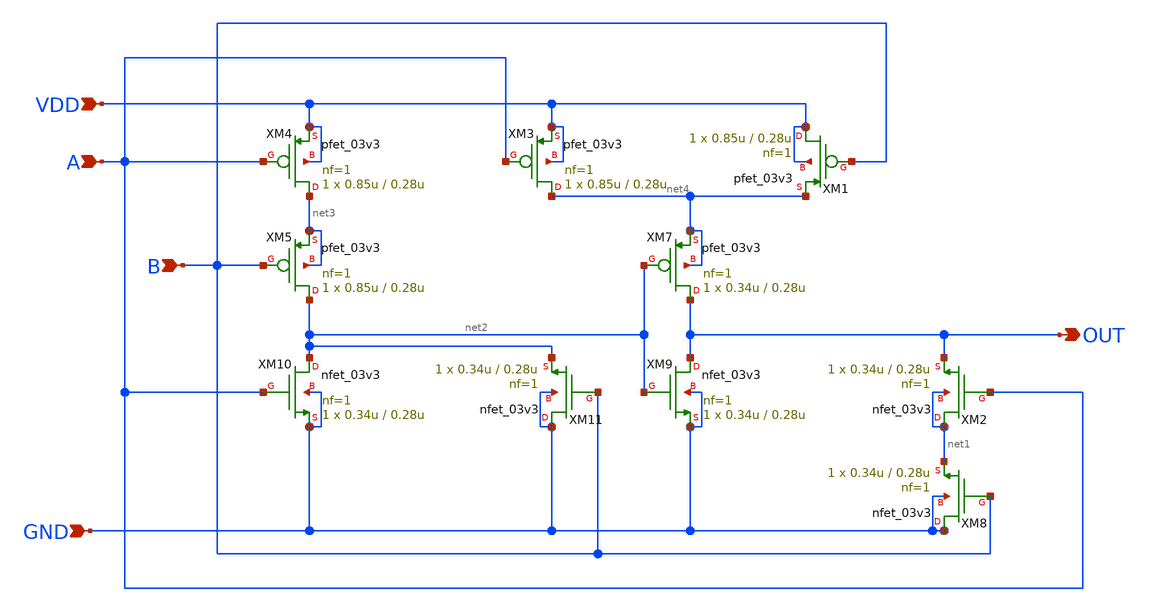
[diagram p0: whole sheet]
** sch_path: Project/1-on-chip/schematic/PNgen/xor.sch
**.subckt xor VDD OUT A B GND
*.ipin VDD
*.opin OUT
*.ipin A
*.ipin B
*.ipin GND
XM7 OUT net2 net4 net4 pfet_03v3 L=0.28u W=0.34u nf=1 ad='int((nf+1)/2) * W/nf * 0.18u' as='int((nf+2)/2) * W/nf * 0.18u'
+ pd='2*int((nf+1)/2) * (W/nf + 0.18u)' ps='2*int((nf+2)/2) * (W/nf + 0.18u)' nrd='0.18u / W' nrs='0.18u / W'
+ sa=0 sb=0 sd=0 m=1
XM1 VDD B net4 VDD pfet_03v3 L=0.28u W=0.85u nf=1 ad='int((nf+1)/2) * W/nf * 0.18u' as='int((nf+2)/2) * W/nf * 0.18u'
+ pd='2*int((nf+1)/2) * (W/nf + 0.18u)' ps='2*int((nf+2)/2) * (W/nf + 0.18u)' nrd='0.18u / W' nrs='0.18u / W'
+ sa=0 sb=0 sd=0 m=1
XM2 net1 A OUT net1 nfet_03v3 L=0.28u W=0.34u nf=1 ad='int((nf+1)/2) * W/nf * 0.18u' as='int((nf+2)/2) * W/nf * 0.18u'
+ pd='2*int((nf+1)/2) * (W/nf + 0.18u)' ps='2*int((nf+2)/2) * (W/nf + 0.18u)' nrd='0.18u / W' nrs='0.18u / W'
+ sa=0 sb=0 sd=0 m=1
XM8 GND B net1 GND nfet_03v3 L=0.28u W=0.34u nf=1 ad='int((nf+1)/2) * W/nf * 0.18u' as='int((nf+2)/2) * W/nf * 0.18u'
+ pd='2*int((nf+1)/2) * (W/nf + 0.18u)' ps='2*int((nf+2)/2) * (W/nf + 0.18u)' nrd='0.18u / W' nrs='0.18u / W'
+ sa=0 sb=0 sd=0 m=1
XM9 OUT net2 GND GND nfet_03v3 L=0.28u W=0.34u nf=1 ad='int((nf+1)/2) * W/nf * 0.18u' as='int((nf+2)/2) * W/nf * 0.18u'
+ pd='2*int((nf+1)/2) * (W/nf + 0.18u)' ps='2*int((nf+2)/2) * (W/nf + 0.18u)' nrd='0.18u / W' nrs='0.18u / W'
+ sa=0 sb=0 sd=0 m=1
XM10 net2 A GND GND nfet_03v3 L=0.28u W=0.34u nf=1 ad='int((nf+1)/2) * W/nf * 0.18u' as='int((nf+2)/2) * W/nf * 0.18u'
+ pd='2*int((nf+1)/2) * (W/nf + 0.18u)' ps='2*int((nf+2)/2) * (W/nf + 0.18u)' nrd='0.18u / W' nrs='0.18u / W'
+ sa=0 sb=0 sd=0 m=1
XM11 GND B net2 GND nfet_03v3 L=0.28u W=0.34u nf=1 ad='int((nf+1)/2) * W/nf * 0.18u' as='int((nf+2)/2) * W/nf * 0.18u'
+ pd='2*int((nf+1)/2) * (W/nf + 0.18u)' ps='2*int((nf+2)/2) * (W/nf + 0.18u)' nrd='0.18u / W' nrs='0.18u / W'
+ sa=0 sb=0 sd=0 m=1
XM3 net4 A VDD VDD pfet_03v3 L=0.28u W=0.85u nf=1 ad='int((nf+1)/2) * W/nf * 0.18u' as='int((nf+2)/2) * W/nf * 0.18u'
+ pd='2*int((nf+1)/2) * (W/nf + 0.18u)' ps='2*int((nf+2)/2) * (W/nf + 0.18u)' nrd='0.18u / W' nrs='0.18u / W'
+ sa=0 sb=0 sd=0 m=1
XM4 net3 A VDD VDD pfet_03v3 L=0.28u W=0.85u nf=1 ad='int((nf+1)/2) * W/nf * 0.18u' as='int((nf+2)/2) * W/nf * 0.18u'
+ pd='2*int((nf+1)/2) * (W/nf + 0.18u)' ps='2*int((nf+2)/2) * (W/nf + 0.18u)' nrd='0.18u / W' nrs='0.18u / W'
+ sa=0 sb=0 sd=0 m=1
XM5 net2 B net3 net3 pfet_03v3 L=0.28u W=0.85u nf=1 ad='int((nf+1)/2) * W/nf * 0.18u' as='int((nf+2)/2) * W/nf * 0.18u'
+ pd='2*int((nf+1)/2) * (W/nf + 0.18u)' ps='2*int((nf+2)/2) * (W/nf + 0.18u)' nrd='0.18u / W' nrs='0.18u / W'
+ sa=0 sb=0 sd=0 m=1
**.ends
.end
